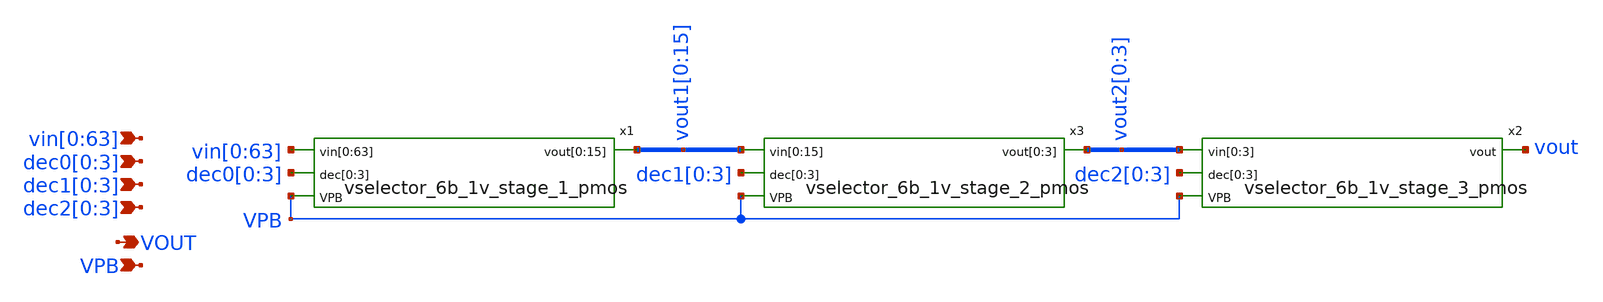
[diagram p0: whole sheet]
** sch_path: xschem/vselector_6b_1v_pmos.sch
**.subckt vselector_6b_1v_pmos
*+ vin[0],vin[1],vin[2],vin[3],vin[4],vin[5],vin[6],vin[7],vin[8],vin[9],vin[10],vin[11],vin[12],vin[13],vin[14],vin[15],vin[16],vin[17],vin[18],vin[19],vin[20],vin[21],vin[22],vin[23],vin[24],vin[25],vin[26],vin[27],vin[28],vin[29],vin[30],vin[31],vin[32],vin[33],vin[34],vin[35],vin[36],vin[37],vin[38],vin[39],vin[40],vin[41],vin[42],vin[43],vin[44],vin[45],vin[46],vin[47],vin[48],vin[49],vin[50],vin[51],vin[52],vin[53],vin[54],vin[55],vin[56],vin[57],vin[58],vin[59],vin[60],vin[61],vin[62],vin[63] VOUT VPB dec0[0],dec0[1],dec0[2],dec0[3] dec1[0],dec1[1],dec1[2],dec1[3]
*+ dec2[0],dec2[1],dec2[2],dec2[3]
*.ipin
*+ vin[0],vin[1],vin[2],vin[3],vin[4],vin[5],vin[6],vin[7],vin[8],vin[9],vin[10],vin[11],vin[12],vin[13],vin[14],vin[15],vin[16],vin[17],vin[18],vin[19],vin[20],vin[21],vin[22],vin[23],vin[24],vin[25],vin[26],vin[27],vin[28],vin[29],vin[30],vin[31],vin[32],vin[33],vin[34],vin[35],vin[36],vin[37],vin[38],vin[39],vin[40],vin[41],vin[42],vin[43],vin[44],vin[45],vin[46],vin[47],vin[48],vin[49],vin[50],vin[51],vin[52],vin[53],vin[54],vin[55],vin[56],vin[57],vin[58],vin[59],vin[60],vin[61],vin[62],vin[63]
*.opin VOUT
*.ipin VPB
*.ipin dec0[0],dec0[1],dec0[2],dec0[3]
*.ipin dec1[0],dec1[1],dec1[2],dec1[3]
*.ipin dec2[0],dec2[1],dec2[2],dec2[3]
x1 vin[0] vin[1] vin[2] vin[3] vin[4] vin[5] vin[6] vin[7] vin[8] vin[9] vin[10] vin[11] vin[12]
+ vin[13] vin[14] vin[15] vin[16] vin[17] vin[18] vin[19] vin[20] vin[21] vin[22] vin[23] vin[24] vin[25]
+ vin[26] vin[27] vin[28] vin[29] vin[30] vin[31] vin[32] vin[33] vin[34] vin[35] vin[36] vin[37] vin[38]
+ vin[39] vin[40] vin[41] vin[42] vin[43] vin[44] vin[45] vin[46] vin[47] vin[48] vin[49] vin[50] vin[51]
+ vin[52] vin[53] vin[54] vin[55] vin[56] vin[57] vin[58] vin[59] vin[60] vin[61] vin[62] vin[63] dec0[0]
+ dec0[1] dec0[2] dec0[3] vout1[0] vout1[1] vout1[2] vout1[3] vout1[4] vout1[5] vout1[6] vout1[7] vout1[8]
+ vout1[9] vout1[10] vout1[11] vout1[12] vout1[13] vout1[14] vout1[15] VPB vselector_6b_1v_stage_1_pmos
x3 vout1[0] vout1[1] vout1[2] vout1[3] vout1[4] vout1[5] vout1[6] vout1[7] vout1[8] vout1[9]
+ vout1[10] vout1[11] vout1[12] vout1[13] vout1[14] vout1[15] dec1[0] dec1[1] dec1[2] dec1[3] vout2[0] vout2[1]
+ vout2[2] vout2[3] VPB vselector_6b_1v_stage_2_pmos
x2 vout2[0] vout2[1] vout2[2] vout2[3] dec2[0] dec2[1] dec2[2] dec2[3] vout VPB
+ vselector_6b_1v_stage_3_pmos
**.ends

* expanding   symbol:  vselector_6b_1v_stage_1_pmos.sym # of pins=4
** sym_path: xschem/vselector_6b_1v_stage_1_pmos.sym
** sch_path: xschem/vselector_6b_1v_stage_1_pmos.sch
.subckt vselector_6b_1v_stage_1_pmos vin[0] vin[1] vin[2] vin[3] vin[4] vin[5] vin[6] vin[7] vin[8]
+ vin[9] vin[10] vin[11] vin[12] vin[13] vin[14] vin[15] vin[16] vin[17] vin[18] vin[19] vin[20] vin[21]
+ vin[22] vin[23] vin[24] vin[25] vin[26] vin[27] vin[28] vin[29] vin[30] vin[31] vin[32] vin[33] vin[34]
+ vin[35] vin[36] vin[37] vin[38] vin[39] vin[40] vin[41] vin[42] vin[43] vin[44] vin[45] vin[46] vin[47]
+ vin[48] vin[49] vin[50] vin[51] vin[52] vin[53] vin[54] vin[55] vin[56] vin[57] vin[58] vin[59] vin[60]
+ vin[61] vin[62] vin[63] dec[0] dec[1] dec[2] dec[3] vout[0] vout[1] vout[2] vout[3] vout[4] vout[5] vout[6]
+ vout[7] vout[8] vout[9] vout[10] vout[11] vout[12] vout[13] vout[14] vout[15] VPB
*.ipin
*+ vin[0],vin[1],vin[2],vin[3],vin[4],vin[5],vin[6],vin[7],vin[8],vin[9],vin[10],vin[11],vin[12],vin[13],vin[14],vin[15],vin[16],vin[17],vin[18],vin[19],vin[20],vin[21],vin[22],vin[23],vin[24],vin[25],vin[26],vin[27],vin[28],vin[29],vin[30],vin[31],vin[32],vin[33],vin[34],vin[35],vin[36],vin[37],vin[38],vin[39],vin[40],vin[41],vin[42],vin[43],vin[44],vin[45],vin[46],vin[47],vin[48],vin[49],vin[50],vin[51],vin[52],vin[53],vin[54],vin[55],vin[56],vin[57],vin[58],vin[59],vin[60],vin[61],vin[62],vin[63]
*.opin
*+ vout[0],vout[1],vout[2],vout[3],vout[4],vout[5],vout[6],vout[7],vout[8],vout[9],vout[10],vout[11],vout[12],vout[13],vout[14],vout[15]
*.ipin VPB
*.ipin dec[0],dec[1],dec[2],dec[3]
x1 vin[0] vin[1] vin[2] vin[3] vin[4] vin[5] vin[6] vin[7] vin[8] vin[9] vin[10] vin[11] vin[12]
+ vin[13] vin[14] vin[15] dec[0] vout[0] vout[1] vout[2] vout[3] vout[4] vout[5] vout[6] vout[7] vout[8]
+ vout[9] vout[10] vout[11] vout[12] vout[13] vout[14] vout[15] VPB vselector_16b_1v_pmos
x2 vin[16] vin[17] vin[18] vin[19] vin[20] vin[21] vin[22] vin[23] vin[24] vin[25] vin[26] vin[27]
+ vin[28] vin[29] vin[30] vin[31] dec[1] vout[0] vout[1] vout[2] vout[3] vout[4] vout[5] vout[6] vout[7]
+ vout[8] vout[9] vout[10] vout[11] vout[12] vout[13] vout[14] vout[15] VPB vselector_16b_1v_pmos
x3 vin[32] vin[33] vin[34] vin[35] vin[36] vin[37] vin[38] vin[39] vin[40] vin[41] vin[42] vin[43]
+ vin[44] vin[45] vin[46] vin[47] dec[2] vout[0] vout[1] vout[2] vout[3] vout[4] vout[5] vout[6] vout[7]
+ vout[8] vout[9] vout[10] vout[11] vout[12] vout[13] vout[14] vout[15] VPB vselector_16b_1v_pmos
x4 vin[48] vin[49] vin[50] vin[51] vin[52] vin[53] vin[54] vin[55] vin[56] vin[57] vin[58] vin[59]
+ vin[60] vin[61] vin[62] vin[63] dec[3] vout[0] vout[1] vout[2] vout[3] vout[4] vout[5] vout[6] vout[7]
+ vout[8] vout[9] vout[10] vout[11] vout[12] vout[13] vout[14] vout[15] VPB vselector_16b_1v_pmos
.ends


* expanding   symbol:  vselector_6b_1v_stage_2_pmos.sym # of pins=4
** sym_path: xschem/vselector_6b_1v_stage_2_pmos.sym
** sch_path: xschem/vselector_6b_1v_stage_2_pmos.sch
.subckt vselector_6b_1v_stage_2_pmos vin[0] vin[1] vin[2] vin[3] vin[4] vin[5] vin[6] vin[7] vin[8]
+ vin[9] vin[10] vin[11] vin[12] vin[13] vin[14] vin[15] dec[0] dec[1] dec[2] dec[3] vout[0] vout[1] vout[2]
+ vout[3] VPB
*.ipin
*+ vin[0],vin[1],vin[2],vin[3],vin[4],vin[5],vin[6],vin[7],vin[8],vin[9],vin[10],vin[11],vin[12],vin[13],vin[14],vin[15]
*.opin vout[0],vout[1],vout[2],vout[3]
*.ipin VPB
*.ipin dec[0],dec[1],dec[2],dec[3]
x1 vin[0] vin[1] vin[2] vin[3] dec[0] vout[0] vout[1] vout[2] vout[3] VPB vselector_4b_1v_pmos
x2 vin[4] vin[5] vin[6] vin[7] dec[1] vout[0] vout[1] vout[2] vout[3] VPB vselector_4b_1v_pmos
x3 vin[8] vin[9] vin[10] vin[11] dec[2] vout[0] vout[1] vout[2] vout[3] VPB vselector_4b_1v_pmos
x4 vin[12] vin[13] vin[14] vin[15] dec[3] vout[0] vout[1] vout[2] vout[3] VPB vselector_4b_1v_pmos
.ends


* expanding   symbol:  vselector_6b_1v_stage_3_pmos.sym # of pins=4
** sym_path: xschem/vselector_6b_1v_stage_3_pmos.sym
** sch_path: xschem/vselector_6b_1v_stage_3_pmos.sch
.subckt vselector_6b_1v_stage_3_pmos vin[0] vin[1] vin[2] vin[3] dec[0] dec[1] dec[2] dec[3] vout
+ VPB
*.ipin vin[0],vin[1],vin[2],vin[3]
*.opin vout
*.ipin VPB
*.ipin dec[0],dec[1],dec[2],dec[3]
.param wp=0.42 wn=0.42 l=0.5

XM1 vout dec[0] vin[0] VPB sky130_fd_pr__pfet_g5v0d10v5 L=l W=wp nf=1 ad='int((nf+1)/2) * W/nf * 0.29'
+ as='int((nf+2)/2) * W/nf * 0.29' pd='2*int((nf+1)/2) * (W/nf + 0.29)' ps='2*int((nf+2)/2) * (W/nf + 0.29)'
+ nrd='0.29 / W' nrs='0.29 / W' sa=0 sb=0 sd=0 mult=1 m=1
XM2 vout dec[1] vin[1] VPB sky130_fd_pr__pfet_g5v0d10v5 L=l W=wp nf=1 ad='int((nf+1)/2) * W/nf * 0.29'
+ as='int((nf+2)/2) * W/nf * 0.29' pd='2*int((nf+1)/2) * (W/nf + 0.29)' ps='2*int((nf+2)/2) * (W/nf + 0.29)'
+ nrd='0.29 / W' nrs='0.29 / W' sa=0 sb=0 sd=0 mult=1 m=1
XM3 vout dec[2] vin[2] VPB sky130_fd_pr__pfet_g5v0d10v5 L=l W=wp nf=1 ad='int((nf+1)/2) * W/nf * 0.29'
+ as='int((nf+2)/2) * W/nf * 0.29' pd='2*int((nf+1)/2) * (W/nf + 0.29)' ps='2*int((nf+2)/2) * (W/nf + 0.29)'
+ nrd='0.29 / W' nrs='0.29 / W' sa=0 sb=0 sd=0 mult=1 m=1
XM4 vout dec[3] vin[3] VPB sky130_fd_pr__pfet_g5v0d10v5 L=l W=wp nf=1 ad='int((nf+1)/2) * W/nf * 0.29'
+ as='int((nf+2)/2) * W/nf * 0.29' pd='2*int((nf+1)/2) * (W/nf + 0.29)' ps='2*int((nf+2)/2) * (W/nf + 0.29)'
+ nrd='0.29 / W' nrs='0.29 / W' sa=0 sb=0 sd=0 mult=1 m=1
.ends


* expanding   symbol:  vselector_16b_1v_pmos.sym # of pins=4
** sym_path: xschem/vselector_16b_1v_pmos.sym
** sch_path: xschem/vselector_16b_1v_pmos.sch
.subckt vselector_16b_1v_pmos vin[0] vin[1] vin[2] vin[3] vin[4] vin[5] vin[6] vin[7] vin[8] vin[9]
+ vin[10] vin[11] vin[12] vin[13] vin[14] vin[15] DIN vout[0] vout[1] vout[2] vout[3] vout[4] vout[5] vout[6]
+ vout[7] vout[8] vout[9] vout[10] vout[11] vout[12] vout[13] vout[14] vout[15] VPB
*.ipin
*+ vin[0],vin[1],vin[2],vin[3],vin[4],vin[5],vin[6],vin[7],vin[8],vin[9],vin[10],vin[11],vin[12],vin[13],vin[14],vin[15]
*.opin
*+ vout[0],vout[1],vout[2],vout[3],vout[4],vout[5],vout[6],vout[7],vout[8],vout[9],vout[10],vout[11],vout[12],vout[13],vout[14],vout[15]
*.ipin VPB
*.ipin DIN
.param wp=0.42 wn=0.42 l=0.5

XM1 vout[0] DIN vin[0] VPB sky130_fd_pr__pfet_g5v0d10v5 L=l W=wp nf=1 ad='int((nf+1)/2) * W/nf * 0.29'
+ as='int((nf+2)/2) * W/nf * 0.29' pd='2*int((nf+1)/2) * (W/nf + 0.29)' ps='2*int((nf+2)/2) * (W/nf + 0.29)'
+ nrd='0.29 / W' nrs='0.29 / W' sa=0 sb=0 sd=0 mult=1 m=1
XM2 vout[1] DIN vin[1] VPB sky130_fd_pr__pfet_g5v0d10v5 L=l W=wp nf=1 ad='int((nf+1)/2) * W/nf * 0.29'
+ as='int((nf+2)/2) * W/nf * 0.29' pd='2*int((nf+1)/2) * (W/nf + 0.29)' ps='2*int((nf+2)/2) * (W/nf + 0.29)'
+ nrd='0.29 / W' nrs='0.29 / W' sa=0 sb=0 sd=0 mult=1 m=1
XM3 vout[2] DIN vin[2] VPB sky130_fd_pr__pfet_g5v0d10v5 L=l W=wp nf=1 ad='int((nf+1)/2) * W/nf * 0.29'
+ as='int((nf+2)/2) * W/nf * 0.29' pd='2*int((nf+1)/2) * (W/nf + 0.29)' ps='2*int((nf+2)/2) * (W/nf + 0.29)'
+ nrd='0.29 / W' nrs='0.29 / W' sa=0 sb=0 sd=0 mult=1 m=1
XM4 vout[3] DIN vin[3] VPB sky130_fd_pr__pfet_g5v0d10v5 L=l W=wp nf=1 ad='int((nf+1)/2) * W/nf * 0.29'
+ as='int((nf+2)/2) * W/nf * 0.29' pd='2*int((nf+1)/2) * (W/nf + 0.29)' ps='2*int((nf+2)/2) * (W/nf + 0.29)'
+ nrd='0.29 / W' nrs='0.29 / W' sa=0 sb=0 sd=0 mult=1 m=1
XM5 vout[4] DIN vin[4] VPB sky130_fd_pr__pfet_g5v0d10v5 L=l W=wp nf=1 ad='int((nf+1)/2) * W/nf * 0.29'
+ as='int((nf+2)/2) * W/nf * 0.29' pd='2*int((nf+1)/2) * (W/nf + 0.29)' ps='2*int((nf+2)/2) * (W/nf + 0.29)'
+ nrd='0.29 / W' nrs='0.29 / W' sa=0 sb=0 sd=0 mult=1 m=1
XM6 vout[5] DIN vin[5] VPB sky130_fd_pr__pfet_g5v0d10v5 L=l W=wp nf=1 ad='int((nf+1)/2) * W/nf * 0.29'
+ as='int((nf+2)/2) * W/nf * 0.29' pd='2*int((nf+1)/2) * (W/nf + 0.29)' ps='2*int((nf+2)/2) * (W/nf + 0.29)'
+ nrd='0.29 / W' nrs='0.29 / W' sa=0 sb=0 sd=0 mult=1 m=1
XM7 vout[6] DIN vin[6] VPB sky130_fd_pr__pfet_g5v0d10v5 L=l W=wp nf=1 ad='int((nf+1)/2) * W/nf * 0.29'
+ as='int((nf+2)/2) * W/nf * 0.29' pd='2*int((nf+1)/2) * (W/nf + 0.29)' ps='2*int((nf+2)/2) * (W/nf + 0.29)'
+ nrd='0.29 / W' nrs='0.29 / W' sa=0 sb=0 sd=0 mult=1 m=1
XM8 vout[7] DIN vin[7] VPB sky130_fd_pr__pfet_g5v0d10v5 L=l W=wp nf=1 ad='int((nf+1)/2) * W/nf * 0.29'
+ as='int((nf+2)/2) * W/nf * 0.29' pd='2*int((nf+1)/2) * (W/nf + 0.29)' ps='2*int((nf+2)/2) * (W/nf + 0.29)'
+ nrd='0.29 / W' nrs='0.29 / W' sa=0 sb=0 sd=0 mult=1 m=1
XM9 vout[8] DIN vin[8] VPB sky130_fd_pr__pfet_g5v0d10v5 L=l W=wp nf=1 ad='int((nf+1)/2) * W/nf * 0.29'
+ as='int((nf+2)/2) * W/nf * 0.29' pd='2*int((nf+1)/2) * (W/nf + 0.29)' ps='2*int((nf+2)/2) * (W/nf + 0.29)'
+ nrd='0.29 / W' nrs='0.29 / W' sa=0 sb=0 sd=0 mult=1 m=1
XM10 vout[9] DIN vin[9] VPB sky130_fd_pr__pfet_g5v0d10v5 L=l W=wp nf=1 ad='int((nf+1)/2) * W/nf * 0.29'
+ as='int((nf+2)/2) * W/nf * 0.29' pd='2*int((nf+1)/2) * (W/nf + 0.29)' ps='2*int((nf+2)/2) * (W/nf + 0.29)'
+ nrd='0.29 / W' nrs='0.29 / W' sa=0 sb=0 sd=0 mult=1 m=1
XM11 vout[10] DIN vin[10] VPB sky130_fd_pr__pfet_g5v0d10v5 L=l W=wp nf=1 ad='int((nf+1)/2) * W/nf * 0.29'
+ as='int((nf+2)/2) * W/nf * 0.29' pd='2*int((nf+1)/2) * (W/nf + 0.29)' ps='2*int((nf+2)/2) * (W/nf + 0.29)'
+ nrd='0.29 / W' nrs='0.29 / W' sa=0 sb=0 sd=0 mult=1 m=1
XM12 vout[11] DIN vin[11] VPB sky130_fd_pr__pfet_g5v0d10v5 L=l W=wp nf=1 ad='int((nf+1)/2) * W/nf * 0.29'
+ as='int((nf+2)/2) * W/nf * 0.29' pd='2*int((nf+1)/2) * (W/nf + 0.29)' ps='2*int((nf+2)/2) * (W/nf + 0.29)'
+ nrd='0.29 / W' nrs='0.29 / W' sa=0 sb=0 sd=0 mult=1 m=1
XM13 vout[12] DIN vin[12] VPB sky130_fd_pr__pfet_g5v0d10v5 L=l W=wp nf=1 ad='int((nf+1)/2) * W/nf * 0.29'
+ as='int((nf+2)/2) * W/nf * 0.29' pd='2*int((nf+1)/2) * (W/nf + 0.29)' ps='2*int((nf+2)/2) * (W/nf + 0.29)'
+ nrd='0.29 / W' nrs='0.29 / W' sa=0 sb=0 sd=0 mult=1 m=1
XM14 vout[13] DIN vin[13] VPB sky130_fd_pr__pfet_g5v0d10v5 L=l W=wp nf=1 ad='int((nf+1)/2) * W/nf * 0.29'
+ as='int((nf+2)/2) * W/nf * 0.29' pd='2*int((nf+1)/2) * (W/nf + 0.29)' ps='2*int((nf+2)/2) * (W/nf + 0.29)'
+ nrd='0.29 / W' nrs='0.29 / W' sa=0 sb=0 sd=0 mult=1 m=1
XM15 vout[14] DIN vin[14] VPB sky130_fd_pr__pfet_g5v0d10v5 L=l W=wp nf=1 ad='int((nf+1)/2) * W/nf * 0.29'
+ as='int((nf+2)/2) * W/nf * 0.29' pd='2*int((nf+1)/2) * (W/nf + 0.29)' ps='2*int((nf+2)/2) * (W/nf + 0.29)'
+ nrd='0.29 / W' nrs='0.29 / W' sa=0 sb=0 sd=0 mult=1 m=1
XM16 vout[15] DIN vin[15] VPB sky130_fd_pr__pfet_g5v0d10v5 L=l W=wp nf=1 ad='int((nf+1)/2) * W/nf * 0.29'
+ as='int((nf+2)/2) * W/nf * 0.29' pd='2*int((nf+1)/2) * (W/nf + 0.29)' ps='2*int((nf+2)/2) * (W/nf + 0.29)'
+ nrd='0.29 / W' nrs='0.29 / W' sa=0 sb=0 sd=0 mult=1 m=1
.ends


* expanding   symbol:  vselector_4b_1v_pmos.sym # of pins=4
** sym_path: xschem/vselector_4b_1v_pmos.sym
** sch_path: xschem/vselector_4b_1v_pmos.sch
.subckt vselector_4b_1v_pmos vin[0] vin[1] vin[2] vin[3] DIN vout[0] vout[1] vout[2] vout[3] VPB
*.ipin vin[0],vin[1],vin[2],vin[3]
*.opin vout[0],vout[1],vout[2],vout[3]
*.ipin VPB
*.ipin DIN
.param wp=0.42 wn=0.42 l=0.5

XM1 vout[0] DIN vin[0] VPB sky130_fd_pr__pfet_g5v0d10v5 L=l W=wp nf=1 ad='int((nf+1)/2) * W/nf * 0.29'
+ as='int((nf+2)/2) * W/nf * 0.29' pd='2*int((nf+1)/2) * (W/nf + 0.29)' ps='2*int((nf+2)/2) * (W/nf + 0.29)'
+ nrd='0.29 / W' nrs='0.29 / W' sa=0 sb=0 sd=0 mult=1 m=1
XM2 vout[1] DIN vin[1] VPB sky130_fd_pr__pfet_g5v0d10v5 L=l W=wp nf=1 ad='int((nf+1)/2) * W/nf * 0.29'
+ as='int((nf+2)/2) * W/nf * 0.29' pd='2*int((nf+1)/2) * (W/nf + 0.29)' ps='2*int((nf+2)/2) * (W/nf + 0.29)'
+ nrd='0.29 / W' nrs='0.29 / W' sa=0 sb=0 sd=0 mult=1 m=1
XM3 vout[2] DIN vin[2] VPB sky130_fd_pr__pfet_g5v0d10v5 L=l W=wp nf=1 ad='int((nf+1)/2) * W/nf * 0.29'
+ as='int((nf+2)/2) * W/nf * 0.29' pd='2*int((nf+1)/2) * (W/nf + 0.29)' ps='2*int((nf+2)/2) * (W/nf + 0.29)'
+ nrd='0.29 / W' nrs='0.29 / W' sa=0 sb=0 sd=0 mult=1 m=1
XM4 vout[3] DIN vin[3] VPB sky130_fd_pr__pfet_g5v0d10v5 L=l W=wp nf=1 ad='int((nf+1)/2) * W/nf * 0.29'
+ as='int((nf+2)/2) * W/nf * 0.29' pd='2*int((nf+1)/2) * (W/nf + 0.29)' ps='2*int((nf+2)/2) * (W/nf + 0.29)'
+ nrd='0.29 / W' nrs='0.29 / W' sa=0 sb=0 sd=0 mult=1 m=1
.ends

.end
